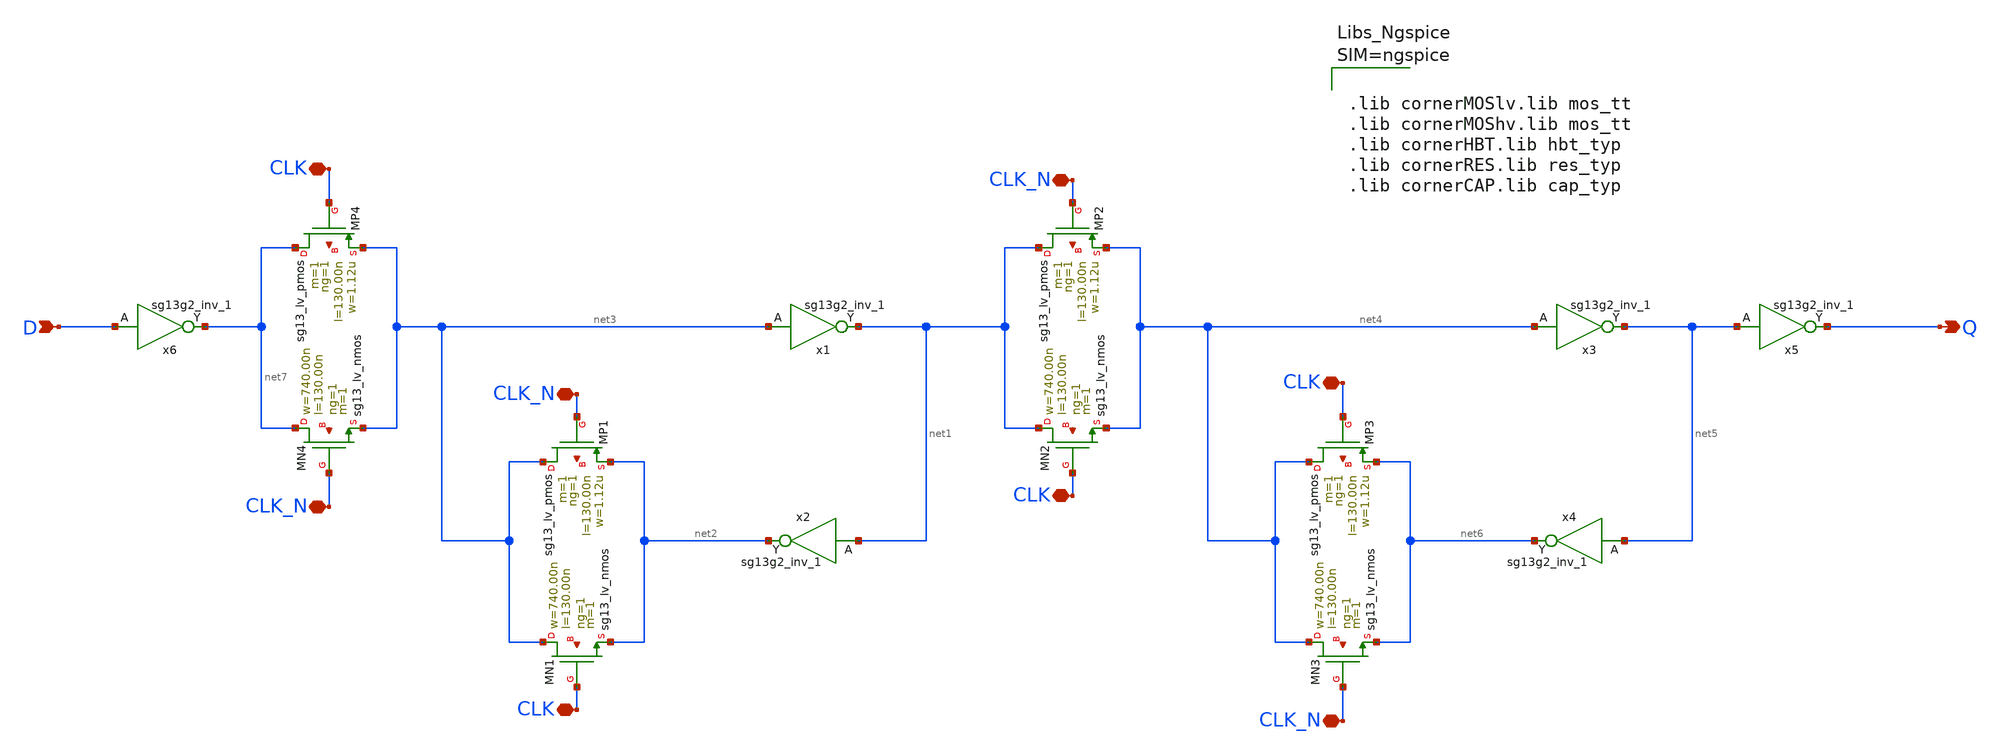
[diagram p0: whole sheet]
** sch_path: xschem/DFF.sch
**.subckt DFF D CLK CLK_N CLK CLK_N CLK CLK_N CLK CLK_N Q
*.ipin D
*.iopin CLK
*.iopin CLK_N
*.iopin CLK
*.iopin CLK_N
*.iopin CLK
*.iopin CLK_N
*.iopin CLK
*.iopin CLK_N
*.opin Q
x1 net1 net3 VDD VSS sg13g2_inv_1
x2 net2 net1 VDD VSS sg13g2_inv_1
XMP1 net3 CLK_N net2 net8 sg13_lv_pmos w=1.12u l=130.00n ng=1 m=1 mm_ok=1
XMN1 net3 CLK net2 net9 sg13_lv_nmos w=740.00n l=130.00n ng=1 m=1 mm_ok=1
XMP2 net1 CLK_N net4 net10 sg13_lv_pmos w=1.12u l=130.00n ng=1 m=1 mm_ok=1
XMN2 net1 CLK net4 net11 sg13_lv_nmos w=740.00n l=130.00n ng=1 m=1 mm_ok=1
x3 net5 net4 VDD VSS sg13g2_inv_1
x4 net6 net5 VDD VSS sg13g2_inv_1
XMP3 net4 CLK net6 net12 sg13_lv_pmos w=1.12u l=130.00n ng=1 m=1 mm_ok=1
XMN3 net4 CLK_N net6 net13 sg13_lv_nmos w=740.00n l=130.00n ng=1 m=1 mm_ok=1
x5 Q net5 VDD VSS sg13g2_inv_1
XMP4 net7 CLK net3 net14 sg13_lv_pmos w=1.12u l=130.00n ng=1 m=1 mm_ok=1
XMN4 net7 CLK_N net3 net15 sg13_lv_nmos w=740.00n l=130.00n ng=1 m=1 mm_ok=1
x6 net7 D VDD VSS sg13g2_inv_1
**** begin user architecture code



.lib cornerMOSlv.lib mos_tt
.lib cornerMOShv.lib mos_tt
.lib cornerHBT.lib hbt_typ
.lib cornerRES.lib res_typ
.lib cornerCAP.lib cap_typ



**** end user architecture code
**.ends

* expanding   symbol:  sg13g2_stdcells/sg13g2_inv_1.sym # of pins=2
** sym_path: sg13g2_stdcells/sg13g2_inv_1.sym
** sch_path: sg13g2_stdcells/sg13g2_inv_1.sch
.subckt sg13g2_inv_1 Y A VDD VSS
*.opin Y
*.ipin A
*.iopin VDD
*.iopin VSS
XM1 Y A VSS VSS sg13_lv_nmos w=740.00n l=130.00n ng=1 m=1 mm_ok=1
XM2 Y A VDD VDD sg13_lv_pmos w=1.12u l=130.00n ng=1 m=1 mm_ok=1
.ends

.end
